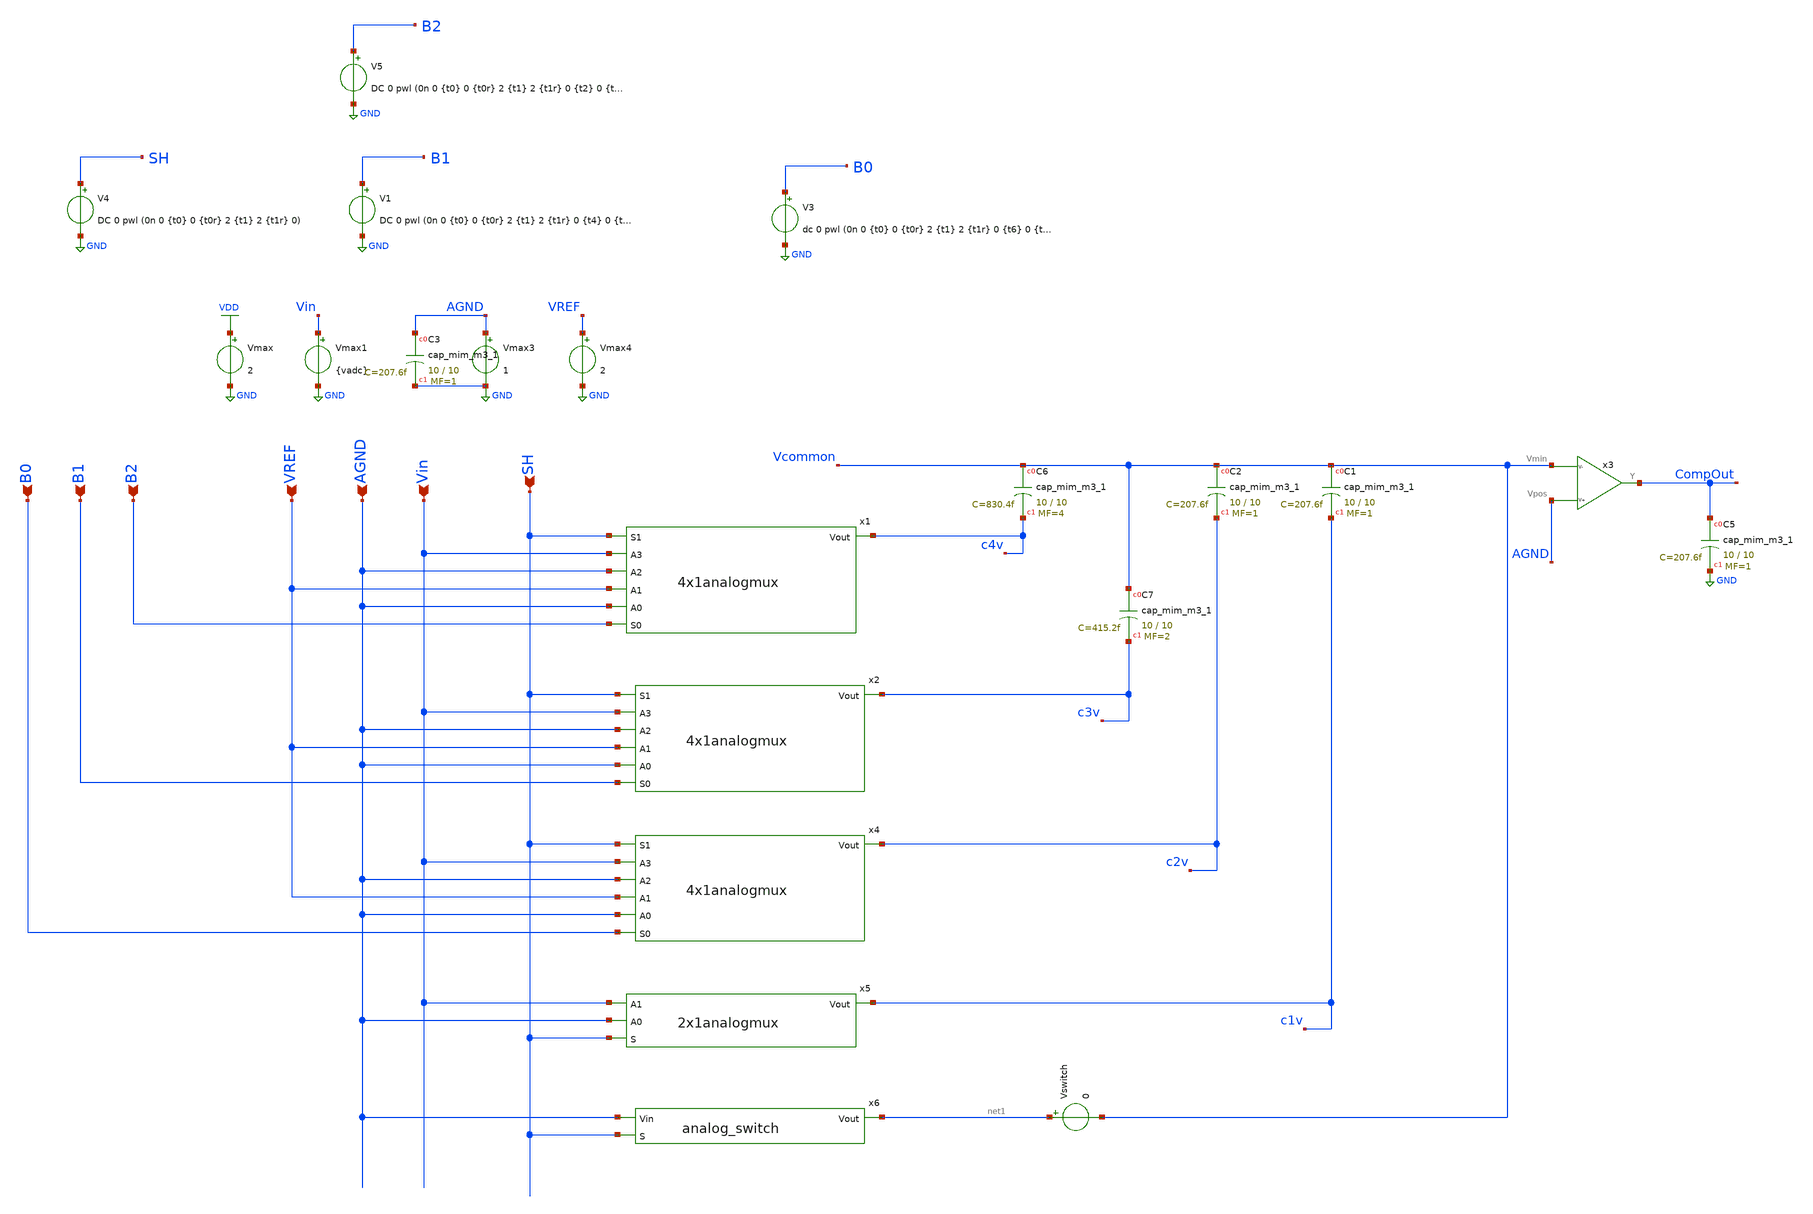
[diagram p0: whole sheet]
** sch_path: dacpassgate_testcircuit_v2.sch
* Copyright 2021 Stefan Frederik Schippers
* Licensed under the Apache License, Version 2.0 (the "License");
* you may not use this file except in compliance with the License.
* You may obtain a copy of the License at
* https://www.apache.org/licenses/LICENSE-2.0
* Unless required by applicable law or agreed to in writing, software
* distributed under the License is distributed on an "AS IS" BASIS,
* WITHOUT WARRANTIES OR CONDITIONS OF ANY KIND, either express or implied.
* See the License for the specific language governing permissions and
* limitations under the License.


.param vONE=2
.param AGND=1
.param rt=5n
.param pw=250n
.param t0=100n
.param t0r=t0+rt
.param t1=t0r+pw
.param t1r=t1+rt
.param t2=t1r+pw
.param t2r=t2+rt
.param t3=t2r+pw
.param t3r=t3+rt
.param t4=t3r+pw
.param t4r=t4+rt
.param t5=t4r+pw
.param t5r=t5+rt
.param t6=t5r+pw
.param t6r=t6+rt
.param t7=t6r+pw
.param t7r=t7+rt
.param b2d=VONE
.param b1d=0
.param b0d=VONE
.param vadc=(b2d/4)+(b1d/8)+(b0d/16)+AGND



**.subckt dacpassgate_testcircuit_v2 Vin AGND VREF SH B0 B1 B2
*.ipin Vin
*.ipin AGND
*.ipin VREF
*.ipin SH
*.ipin B0
*.ipin B1
*.ipin B2
Vmax VDD GND 2
XC1 Vcommon c1v sky130_fd_pr__cap_mim_m3_1 W=10 L=10 MF=1 m=1
Vmax1 Vin GND {vadc}
Vmax3 AGND GND 1
V4 SH GND DC 0 pwl (0n 0 {t0} 0 {t0r} 2 {t1} 2 {t1r} 0)
XC5 CompOut GND sky130_fd_pr__cap_mim_m3_1 W=10 L=10 MF=1 m=1
Vmax4 VREF GND 2
XC2 Vcommon c2v sky130_fd_pr__cap_mim_m3_1 W=10 L=10 MF=1 m=1
V1 B1 GND DC 0 pwl (0n 0 {t0} 0 {t0r} 2 {t1} 2 {t1r} 0 {t4} 0 {t4r} 2 {t5} 2 {t5r} {b1d})
x3 Vcommon AGND CompOut skywater_comparator
V3 B0 GND dc 0 pwl (0n 0 {t0} 0 {t0r} 2 {t1} 2 {t1r} 0 {t6} 0 {t6r} 2 {t7} 2 {t7r} {b0d})
V5 B2 GND DC 0 pwl (0n 0 {t0} 0 {t0r} 2 {t1} 2 {t1r} 0 {t2} 0 {t2r} 2 {t3} 2 {t3r} {b2d})
XC6 Vcommon c4v sky130_fd_pr__cap_mim_m3_1 W=10 L=10 MF=4 m=4
XC7 Vcommon c3v sky130_fd_pr__cap_mim_m3_1 W=10 L=10 MF=2 m=2
x1 c4v SH Vin AGND VREF AGND B2 4x1analogmux
x2 c3v SH Vin AGND VREF AGND B1 4x1analogmux
x4 c2v SH Vin AGND VREF AGND B0 4x1analogmux
x5 c1v Vin AGND SH 2x1analogmux
x6 AGND SH net1 analog_switch
Vswitch net1 Vcommon 0
XC3 AGND GND sky130_fd_pr__cap_mim_m3_1 W=10 L=10 MF=1 m=1
**** begin user architecture code


.include opamp_subckt.sp

.tran 0.1 2000n
.control
run
**plot i(Vswitch)
write dacpassgate_testcircuit_v2.raw
plot v(SH) v(B0)+2 v(B1)+4 v(B2)+6
plot v(Vin)  v(vCommon)
**plot v(AGND)
plot v(c1v) v(c2v)+2 v(c3v)+4 v(c4v)+6
plot v(CompOut)
.endc



** opencircuitdesign pdks install
.lib $::SKYWATER_MODELS/sky130.lib.spice tt


**** end user architecture code
**.ends
.GLOBAL GND
.GLOBAL VDD
.end
